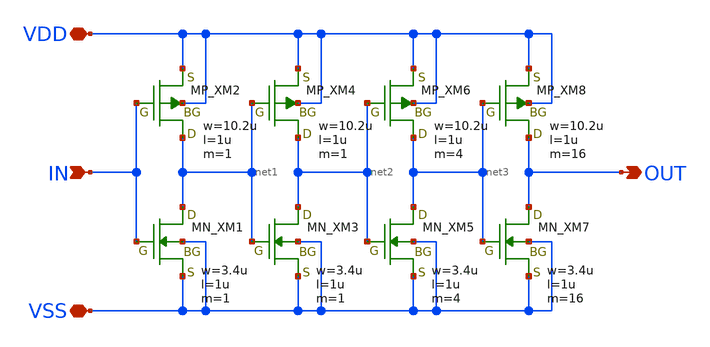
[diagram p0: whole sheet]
** sch_path: member_project/imager/YuMaehashi/design/buf_x16.sch
**.subckt buf_x16 OUT IN VDD VSS
*.opin OUT
*.ipin IN
*.iopin VDD
*.iopin VSS
XXM1 net1 IN VSS VSS NMOS w=3.4u l=1u nrd=0 nrs=0 m=1
XXM2 net1 IN VDD VDD PMOS w=10.2u l=1u nrd=0 nrs=0 m=1
XXM3 net2 net1 VSS VSS NMOS w=3.4u l=1u nrd=0 nrs=0 m=1
XXM4 net2 net1 VDD VDD PMOS w=10.2u l=1u nrd=0 nrs=0 m=1
XXM5 net3 net2 VSS VSS NMOS w=3.4u l=1u nrd=0 nrs=0 m=4
XXM6 net3 net2 VDD VDD PMOS w=10.2u l=1u nrd=0 nrs=0 m=4
XXM7 OUT net3 VSS VSS NMOS w=3.4u l=1u nrd=0 nrs=0 m=16
XXM8 OUT net3 VDD VDD PMOS w=10.2u l=1u nrd=0 nrs=0 m=16
**.ends
.end
